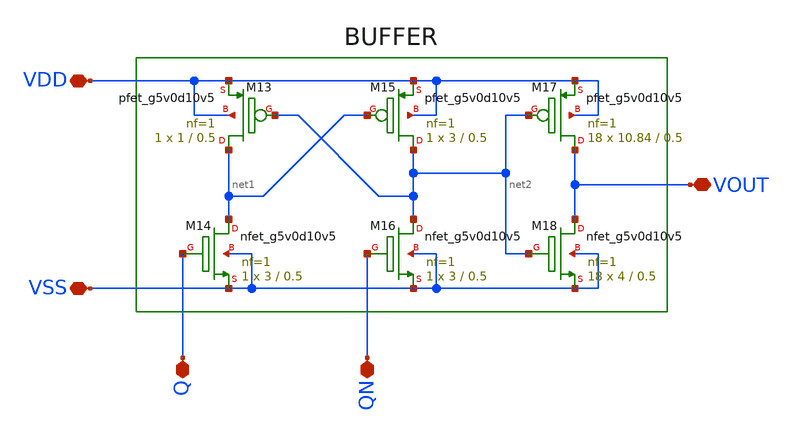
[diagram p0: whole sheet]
** sch_path: xschem/buffer.sch
**.subckt buffer VDD VSS Q QN VOUT
*.iopin VDD
*.iopin VSS
*.iopin Q
*.iopin QN
*.iopin VOUT
XM15 net2 net1 VDD VDD sky130_fd_pr__pfet_g5v0d10v5 L=0.5 W=3 nf=1 ad='int((nf+1)/2) * W/nf * 0.29' as='int((nf+2)/2) * W/nf * 0.29'
+ pd='2*int((nf+1)/2) * (W/nf + 0.29)' ps='2*int((nf+2)/2) * (W/nf + 0.29)' nrd='0.29 / W' nrs='0.29 / W'
+ sa=0 sb=0 sd=0 mult=1 m=1
XM13 net1 net2 VDD VDD sky130_fd_pr__pfet_g5v0d10v5 L=0.5 W=1 nf=1 ad='int((nf+1)/2) * W/nf * 0.29' as='int((nf+2)/2) * W/nf * 0.29'
+ pd='2*int((nf+1)/2) * (W/nf + 0.29)' ps='2*int((nf+2)/2) * (W/nf + 0.29)' nrd='0.29 / W' nrs='0.29 / W'
+ sa=0 sb=0 sd=0 mult=1 m=1
XM17 VOUT net2 VDD VDD sky130_fd_pr__pfet_g5v0d10v5 L=0.5 W=10.84 nf=1 ad='int((nf+1)/2) * W/nf * 0.29'
+ as='int((nf+2)/2) * W/nf * 0.29' pd='2*int((nf+1)/2) * (W/nf + 0.29)' ps='2*int((nf+2)/2) * (W/nf + 0.29)'
+ nrd='0.29 / W' nrs='0.29 / W' sa=0 sb=0 sd=0 mult=18 m=18
XM14 net1 Q VSS VSS sky130_fd_pr__nfet_g5v0d10v5 L=0.5 W=3 nf=1 ad='int((nf+1)/2) * W/nf * 0.29' as='int((nf+2)/2) * W/nf * 0.29'
+ pd='2*int((nf+1)/2) * (W/nf + 0.29)' ps='2*int((nf+2)/2) * (W/nf + 0.29)' nrd='0.29 / W' nrs='0.29 / W'
+ sa=0 sb=0 sd=0 mult=1 m=1
XM16 net2 QN VSS VSS sky130_fd_pr__nfet_g5v0d10v5 L=0.5 W=3 nf=1 ad='int((nf+1)/2) * W/nf * 0.29' as='int((nf+2)/2) * W/nf * 0.29'
+ pd='2*int((nf+1)/2) * (W/nf + 0.29)' ps='2*int((nf+2)/2) * (W/nf + 0.29)' nrd='0.29 / W' nrs='0.29 / W'
+ sa=0 sb=0 sd=0 mult=1 m=1
XM18 VOUT net2 VSS VSS sky130_fd_pr__nfet_g5v0d10v5 L=0.5 W=4 nf=1 ad='int((nf+1)/2) * W/nf * 0.29' as='int((nf+2)/2) * W/nf * 0.29'
+ pd='2*int((nf+1)/2) * (W/nf + 0.29)' ps='2*int((nf+2)/2) * (W/nf + 0.29)' nrd='0.29 / W' nrs='0.29 / W'
+ sa=0 sb=0 sd=0 mult=18 m=18
**.ends
.end
